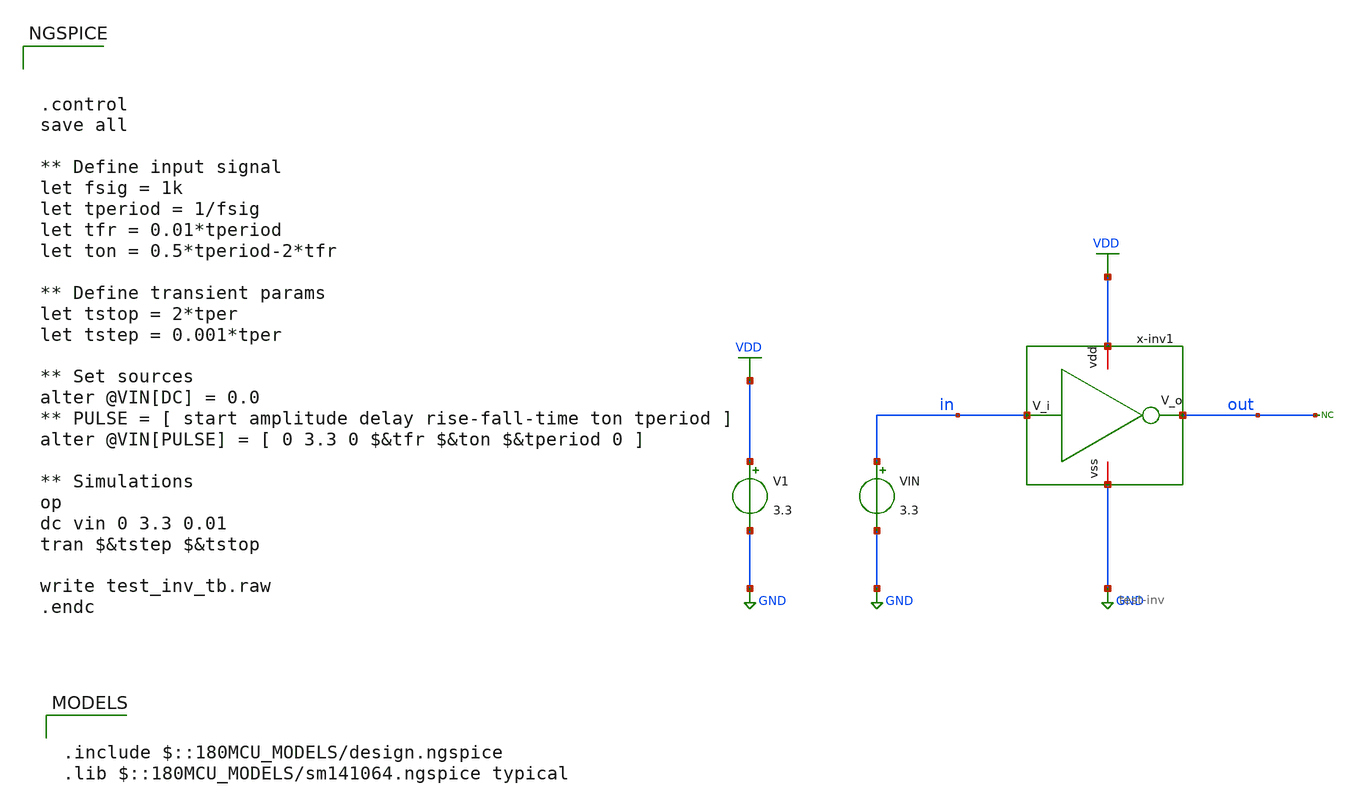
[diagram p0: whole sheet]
** sch_path: designs/test/test-inv_tb.sch
**.subckt test-inv_tb
V1 VDD GND 3.3
VIN in GND 3.3
* noconn out
x-inv1 VDD in out GND test-inv
**** begin user architecture code

.include $::180MCU_MODELS/design.ngspice
.lib $::180MCU_MODELS/sm141064.ngspice typical




.control
save all

** Define input signal
let fsig = 1k
let tperiod = 1/fsig
let tfr = 0.01*tperiod
let ton = 0.5*tperiod-2*tfr

** Define transient params
let tstop = 2*tper
let tstep = 0.001*tper

** Set sources
alter @VIN[DC] = 0.0
** PULSE = [ start amplitude delay rise-fall-time ton tperiod ]
alter @VIN[PULSE] = [ 0 3.3 0 $&tfr $&ton $&tperiod 0 ]

** Simulations
op
dc vin 0 3.3 0.01
tran $&tstep $&tstop

write test_inv_tb.raw
.endc


**** end user architecture code
**.ends

* expanding   symbol:  sscs-chipathon-2025-Digimon/test-inv.sym # of pins=4
** sym_path: designs/test/test-inv.sym
** sch_path: designs/test/test-inv.sch
.subckt test-inv vdd V_i V_o vss
*.iopin vdd
*.iopin vss
*.ipin V_i
*.opin V_o
XM1 V_o V_i vss vss nfet_03v3 L=0.28u W=0.22u nf=1 ad='int((nf+1)/2) * W/nf * 0.18u' as='int((nf+2)/2) * W/nf * 0.18u'
+ pd='2*int((nf+1)/2) * (W/nf + 0.18u)' ps='2*int((nf+2)/2) * (W/nf + 0.18u)' nrd='0.18u / W' nrs='0.18u / W'
+ sa=0 sb=0 sd=0 m=1
XM2 V_o V_i vdd vdd pfet_03v3 L=0.28u W=0.22u nf=1 ad='int((nf+1)/2) * W/nf * 0.18u' as='int((nf+2)/2) * W/nf * 0.18u'
+ pd='2*int((nf+1)/2) * (W/nf + 0.18u)' ps='2*int((nf+2)/2) * (W/nf + 0.18u)' nrd='0.18u / W' nrs='0.18u / W'
+ sa=0 sb=0 sd=0 m=1
.ends

.GLOBAL VDD
.GLOBAL GND
.end
